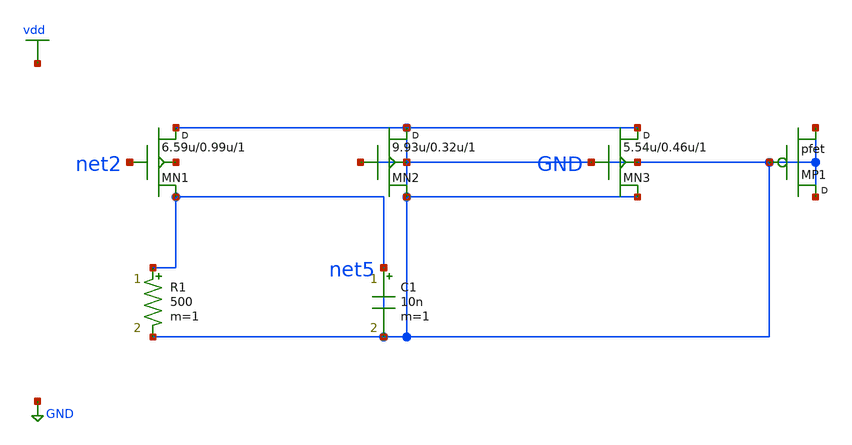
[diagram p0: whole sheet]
** sch_path: synthetic/generated/0030_synthetic.sch
**.subckt 0030_synthetic
MN1 GND net2 GND net1 nfet w=6.59u l=0.99u m=1
MN2 GND GND GND GND nfet w=9.93u l=0.32u m=1
MN3 GND GND GND GND nfet w=5.54u l=0.46u m=1
MP1 GND GND GND pfet m=1
R1 GND GND 500 m=1
C1 GND GND 10n m=1
**.ends
.GLOBAL vdd
.GLOBAL GND
.end
